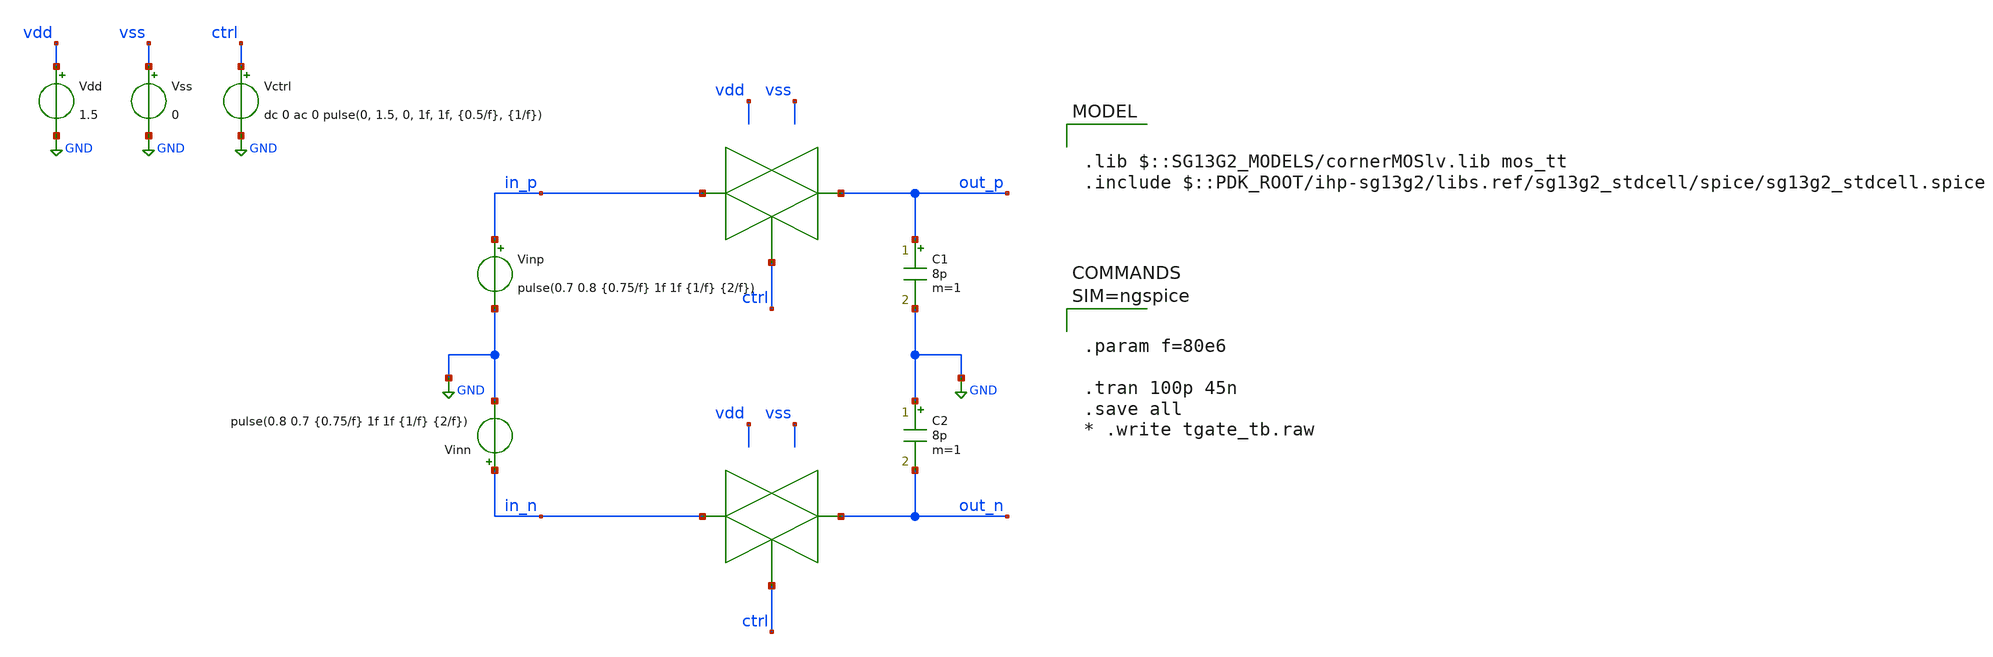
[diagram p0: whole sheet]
** sch_path: designs/tgate_time/tgate_tb.sch
**.subckt tgate_tb
Vdd vdd GND 1.5
Vss vss GND 0
C1 out_p GND 8p m=1
Vinp in_p GND pulse(0.7 0.8 {0.75/f} 1f 1f {1/f} {2/f})
C2 GND out_n 8p m=1
Vinn in_n GND pulse(0.8 0.7 {0.75/f} 1f 1f {1/f} {2/f})
Vctrl ctrl GND dc 0 ac 0 pulse(0, 1.5, 0, 1f, 1f, {0.5/f}, {1/f})
**** begin user architecture code



.param f=80e6

.tran 100p 45n
.save all
* .write tgate_tb.raw




.lib $::SG13G2_MODELS/cornerMOSlv.lib mos_tt
.include $::PDK_ROOT/ihp-sg13g2/libs.ref/sg13g2_stdcell/spice/sg13g2_stdcell.spice

**** end user architecture code
**.ends
.GLOBAL GND
.end
